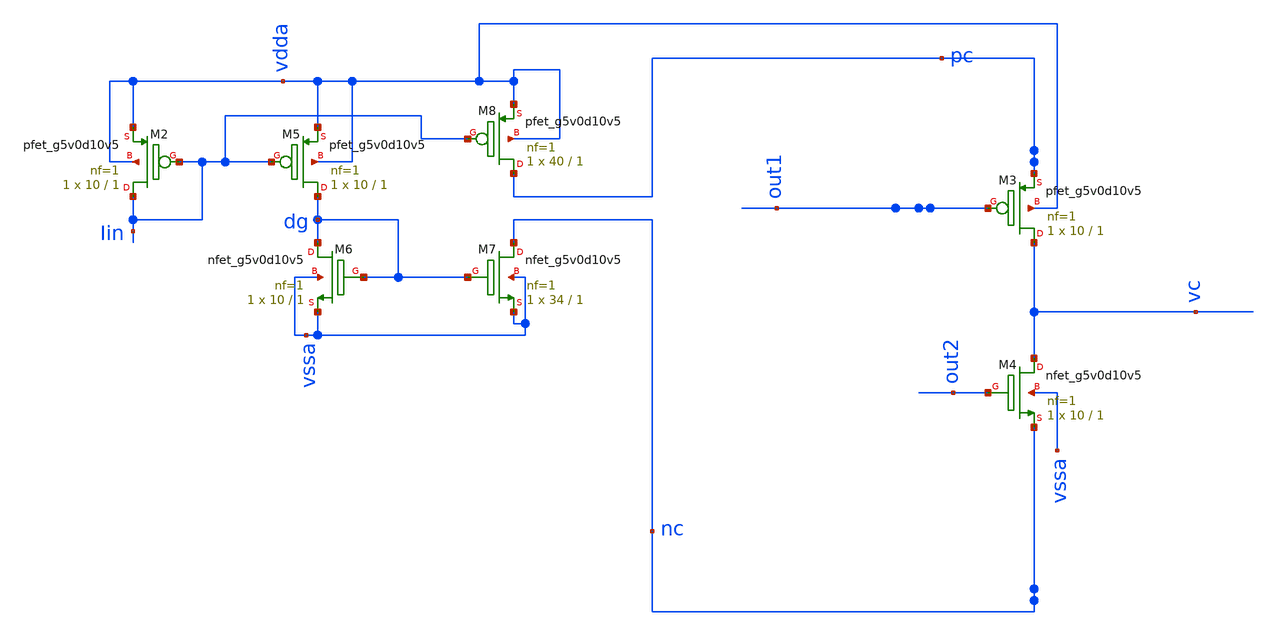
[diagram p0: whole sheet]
** sch_path: xschem/FDC/chargepump_lvs.sch
**.subckt chargepump_lvs
XM3 vc out1 pc vdda sky130_fd_pr__pfet_g5v0d10v5 L=1 W=10 nf=1 ad='int((nf+1)/2) * W/nf * 0.29' as='int((nf+2)/2) * W/nf * 0.29'
+ pd='2*int((nf+1)/2) * (W/nf + 0.29)' ps='2*int((nf+2)/2) * (W/nf + 0.29)' nrd='0.29 / W' nrs='0.29 / W'
+ sa=0 sb=0 sd=0 mult=1 m=1
XM4 vc out2 nc vssa sky130_fd_pr__nfet_g5v0d10v5 L=1 W=10 nf=1 ad='int((nf+1)/2) * W/nf * 0.29' as='int((nf+2)/2) * W/nf * 0.29'
+ pd='2*int((nf+1)/2) * (W/nf + 0.29)' ps='2*int((nf+2)/2) * (W/nf + 0.29)' nrd='0.29 / W' nrs='0.29 / W'
+ sa=0 sb=0 sd=0 mult=1 m=1
XM2 Iin Iin vdda vdda sky130_fd_pr__pfet_g5v0d10v5 L=1 W=10 nf=1 ad='int((nf+1)/2) * W/nf * 0.29' as='int((nf+2)/2) * W/nf * 0.29'
+ pd='2*int((nf+1)/2) * (W/nf + 0.29)' ps='2*int((nf+2)/2) * (W/nf + 0.29)' nrd='0.29 / W' nrs='0.29 / W'
+ sa=0 sb=0 sd=0 mult=1 m=1
XM5 dg Iin vdda vdda sky130_fd_pr__pfet_g5v0d10v5 L=1 W=10 nf=1 ad='int((nf+1)/2) * W/nf * 0.29' as='int((nf+2)/2) * W/nf * 0.29'
+ pd='2*int((nf+1)/2) * (W/nf + 0.29)' ps='2*int((nf+2)/2) * (W/nf + 0.29)' nrd='0.29 / W' nrs='0.29 / W'
+ sa=0 sb=0 sd=0 mult=1 m=1
XM6 dg dg vssa vssa sky130_fd_pr__nfet_g5v0d10v5 L=1 W=10 nf=1 ad='int((nf+1)/2) * W/nf * 0.29' as='int((nf+2)/2) * W/nf * 0.29'
+ pd='2*int((nf+1)/2) * (W/nf + 0.29)' ps='2*int((nf+2)/2) * (W/nf + 0.29)' nrd='0.29 / W' nrs='0.29 / W'
+ sa=0 sb=0 sd=0 mult=1 m=1
XM7 nc dg vssa vssa sky130_fd_pr__nfet_g5v0d10v5 L=1 W=34 nf=1 ad='int((nf+1)/2) * W/nf * 0.29' as='int((nf+2)/2) * W/nf * 0.29'
+ pd='2*int((nf+1)/2) * (W/nf + 0.29)' ps='2*int((nf+2)/2) * (W/nf + 0.29)' nrd='0.29 / W' nrs='0.29 / W'
+ sa=0 sb=0 sd=0 mult=1 m=1
XM8 pc Iin vdda vdda sky130_fd_pr__pfet_g5v0d10v5 L=1 W=40 nf=1 ad='int((nf+1)/2) * W/nf * 0.29' as='int((nf+2)/2) * W/nf * 0.29'
+ pd='2*int((nf+1)/2) * (W/nf + 0.29)' ps='2*int((nf+2)/2) * (W/nf + 0.29)' nrd='0.29 / W' nrs='0.29 / W'
+ sa=0 sb=0 sd=0 mult=1 m=1
**.ends
.end
